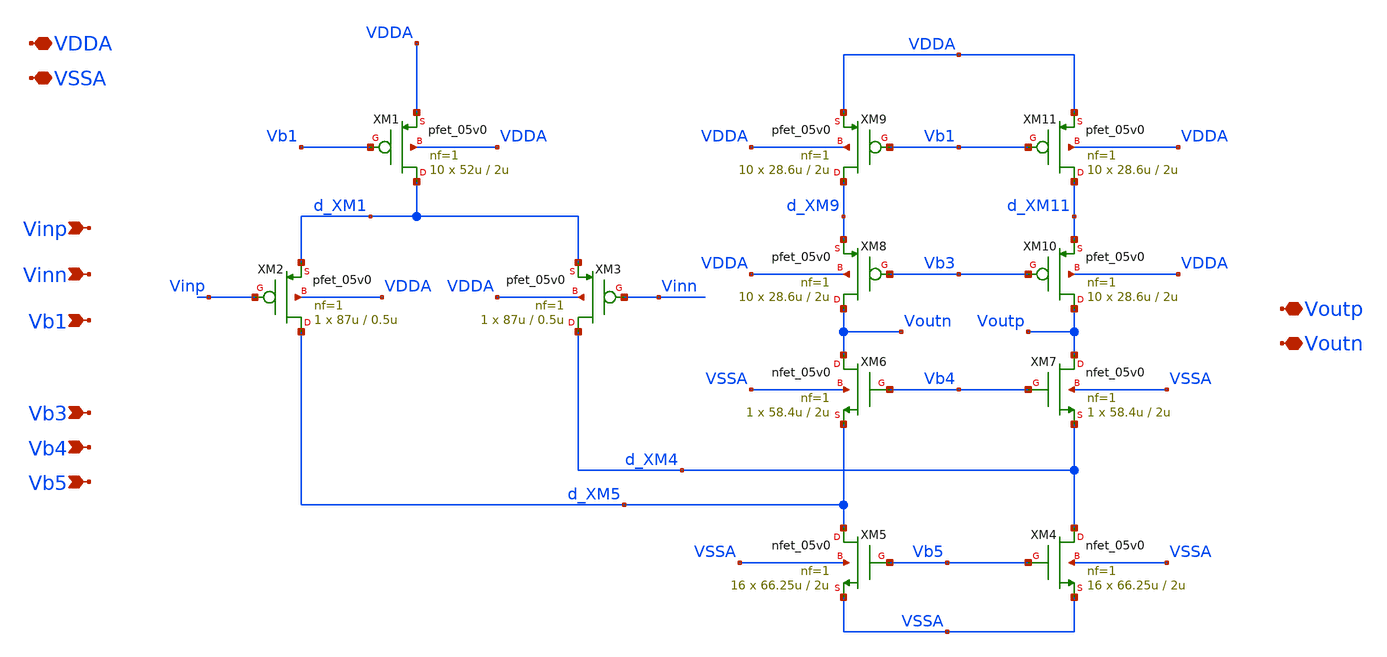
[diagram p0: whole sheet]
** sch_path: schematic/folded_cascode.sch
**.subckt folded_cascode Vinp Vinn VDDA VSSA Vb1 Vb3 Vb4 Vb5 Voutp Voutn
*.ipin Vinp
*.ipin Vinn
*.iopin VDDA
*.iopin VSSA
*.ipin Vb1
*.ipin Vb3
*.ipin Vb4
*.ipin Vb5
*.iopin Voutp
*.iopin Voutn
XM1 d_XM1 Vb1 VDDA VDDA pfet_05v0 L=2u W=52u nf=1 ad='int((nf+1)/2) * W/nf * 0.18u' as='int((nf+2)/2) * W/nf * 0.18u'
+ pd='2*int((nf+1)/2) * (W/nf + 0.18u)' ps='2*int((nf+2)/2) * (W/nf + 0.18u)' nrd='0.18u / W' nrs='0.18u / W'
+ sa=0 sb=0 sd=0 m=10
XM2 d_XM5 Vinp d_XM1 VDDA pfet_05v0 L=0.5u W=87u nf=1 ad='int((nf+1)/2) * W/nf * 0.18u' as='int((nf+2)/2) * W/nf * 0.18u'
+ pd='2*int((nf+1)/2) * (W/nf + 0.18u)' ps='2*int((nf+2)/2) * (W/nf + 0.18u)' nrd='0.18u / W' nrs='0.18u / W'
+ sa=0 sb=0 sd=0 m=1
XM3 d_XM4 Vinn d_XM1 VDDA pfet_05v0 L=0.5u W=87u nf=1 ad='int((nf+1)/2) * W/nf * 0.18u' as='int((nf+2)/2) * W/nf * 0.18u'
+ pd='2*int((nf+1)/2) * (W/nf + 0.18u)' ps='2*int((nf+2)/2) * (W/nf + 0.18u)' nrd='0.18u / W' nrs='0.18u / W'
+ sa=0 sb=0 sd=0 m=1
XM4 d_XM4 Vb5 VSSA VSSA nfet_05v0 L=2u W=66.25u nf=1 ad='int((nf+1)/2) * W/nf * 0.18u' as='int((nf+2)/2) * W/nf * 0.18u'
+ pd='2*int((nf+1)/2) * (W/nf + 0.18u)' ps='2*int((nf+2)/2) * (W/nf + 0.18u)' nrd='0.18u / W' nrs='0.18u / W'
+ sa=0 sb=0 sd=0 m=16
XM5 d_XM5 Vb5 VSSA VSSA nfet_05v0 L=2u W=66.25u nf=1 ad='int((nf+1)/2) * W/nf * 0.18u' as='int((nf+2)/2) * W/nf * 0.18u'
+ pd='2*int((nf+1)/2) * (W/nf + 0.18u)' ps='2*int((nf+2)/2) * (W/nf + 0.18u)' nrd='0.18u / W' nrs='0.18u / W'
+ sa=0 sb=0 sd=0 m=16
XM6 Voutn Vb4 d_XM5 VSSA nfet_05v0 L=2u W=58.4u nf=1 ad='int((nf+1)/2) * W/nf * 0.18u' as='int((nf+2)/2) * W/nf * 0.18u'
+ pd='2*int((nf+1)/2) * (W/nf + 0.18u)' ps='2*int((nf+2)/2) * (W/nf + 0.18u)' nrd='0.18u / W' nrs='0.18u / W'
+ sa=0 sb=0 sd=0 m=1
XM7 Voutp Vb4 d_XM4 VSSA nfet_05v0 L=2u W=58.4u nf=1 ad='int((nf+1)/2) * W/nf * 0.18u' as='int((nf+2)/2) * W/nf * 0.18u'
+ pd='2*int((nf+1)/2) * (W/nf + 0.18u)' ps='2*int((nf+2)/2) * (W/nf + 0.18u)' nrd='0.18u / W' nrs='0.18u / W'
+ sa=0 sb=0 sd=0 m=1
XM8 Voutn Vb3 d_XM9 VDDA pfet_05v0 L=2u W=28.6u nf=1 ad='int((nf+1)/2) * W/nf * 0.18u' as='int((nf+2)/2) * W/nf * 0.18u'
+ pd='2*int((nf+1)/2) * (W/nf + 0.18u)' ps='2*int((nf+2)/2) * (W/nf + 0.18u)' nrd='0.18u / W' nrs='0.18u / W'
+ sa=0 sb=0 sd=0 m=10
XM9 d_XM9 Vb1 VDDA VDDA pfet_05v0 L=2u W=28.6u nf=1 ad='int((nf+1)/2) * W/nf * 0.18u' as='int((nf+2)/2) * W/nf * 0.18u'
+ pd='2*int((nf+1)/2) * (W/nf + 0.18u)' ps='2*int((nf+2)/2) * (W/nf + 0.18u)' nrd='0.18u / W' nrs='0.18u / W'
+ sa=0 sb=0 sd=0 m=10
XM10 Voutp Vb3 d_XM11 VDDA pfet_05v0 L=2u W=28.6u nf=1 ad='int((nf+1)/2) * W/nf * 0.18u' as='int((nf+2)/2) * W/nf * 0.18u'
+ pd='2*int((nf+1)/2) * (W/nf + 0.18u)' ps='2*int((nf+2)/2) * (W/nf + 0.18u)' nrd='0.18u / W' nrs='0.18u / W'
+ sa=0 sb=0 sd=0 m=10
XM11 d_XM11 Vb1 VDDA VDDA pfet_05v0 L=2u W=28.6u nf=1 ad='int((nf+1)/2) * W/nf * 0.18u' as='int((nf+2)/2) * W/nf * 0.18u'
+ pd='2*int((nf+1)/2) * (W/nf + 0.18u)' ps='2*int((nf+2)/2) * (W/nf + 0.18u)' nrd='0.18u / W' nrs='0.18u / W'
+ sa=0 sb=0 sd=0 m=10
**.ends
.end
